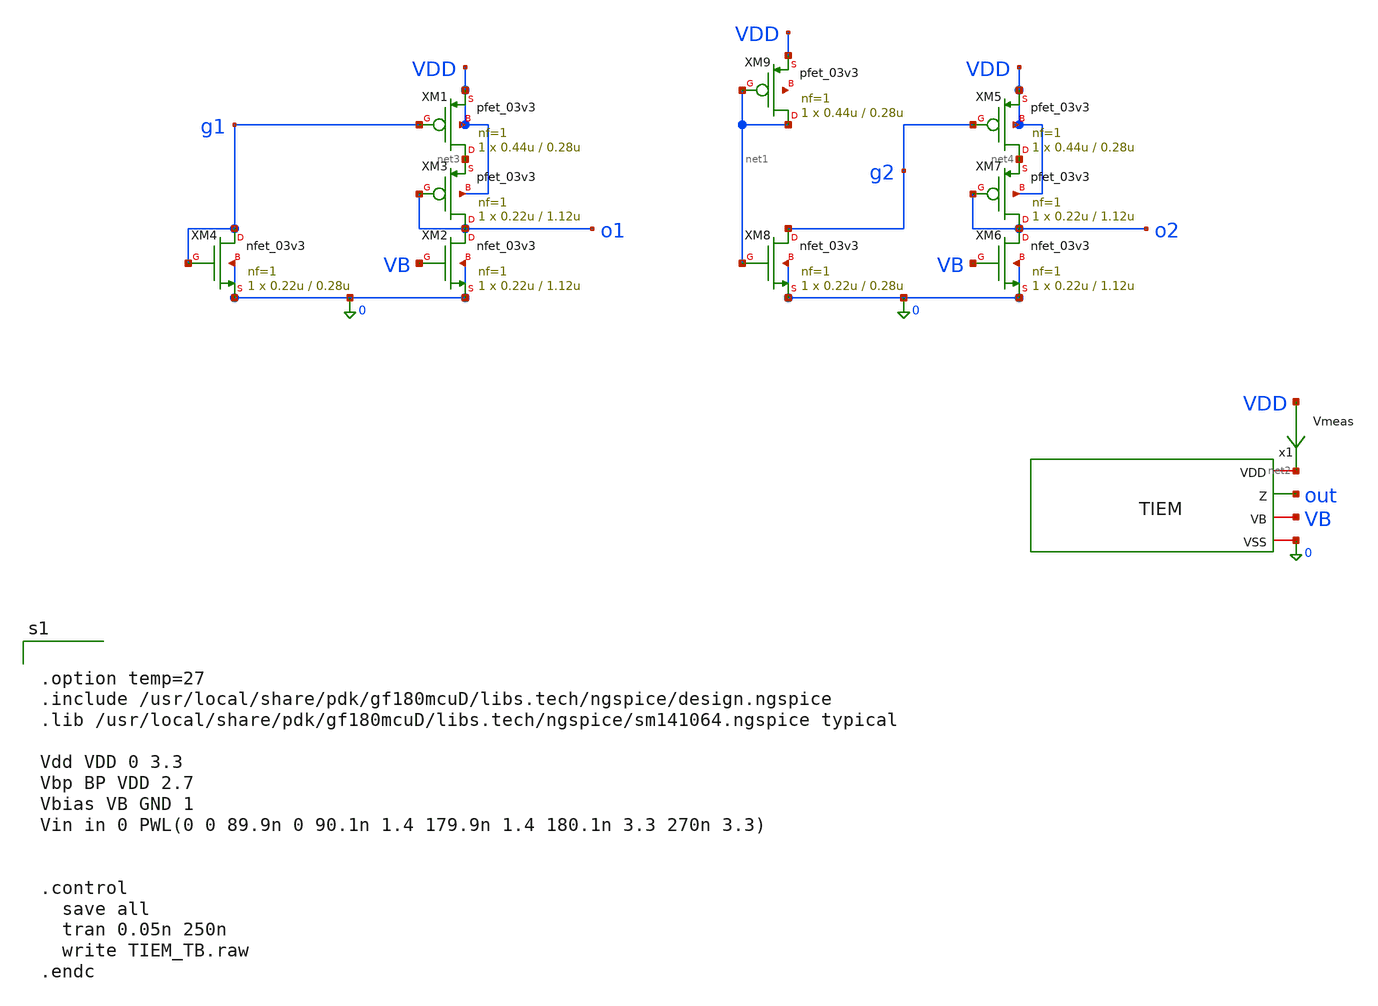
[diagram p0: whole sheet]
** sch_path: xschem_sn2/TIEM_TB.sch
**.subckt TIEM_TB
Vmeas VDD net2 0
.save i(vmeas)
x1 net2 out VB 0 TIEM
XM1 net3 g1 VDD VDD pfet_03v3 L=0.28u W=0.44u nf=1 ad='int((nf+1)/2) * W/nf * 0.18u' as='int((nf+2)/2) * W/nf * 0.18u'
+ pd='2*int((nf+1)/2) * (W/nf + 0.18u)' ps='2*int((nf+2)/2) * (W/nf + 0.18u)' nrd='0.18u / W' nrs='0.18u / W'
+ sa=0 sb=0 sd=0 m=1 par=1
XM2 o1 VB 0 0 nfet_03v3 L=1.12u W=0.22u nf=1 ad='int((nf+1)/2) * W/nf * 0.18u' as='int((nf+2)/2) * W/nf * 0.18u'
+ pd='2*int((nf+1)/2) * (W/nf + 0.18u)' ps='2*int((nf+2)/2) * (W/nf + 0.18u)' nrd='0.18u / W' nrs='0.18u / W'
+ sa=0 sb=0 sd=0 m=1 par=1
XM3 o1 o1 net3 VDD pfet_03v3 L=1.12u W=0.22u nf=1 ad='int((nf+1)/2) * W/nf * 0.18u' as='int((nf+2)/2) * W/nf * 0.18u'
+ pd='2*int((nf+1)/2) * (W/nf + 0.18u)' ps='2*int((nf+2)/2) * (W/nf + 0.18u)' nrd='0.18u / W' nrs='0.18u / W'
+ sa=0 sb=0 sd=0 m=1 par=1
XM4 g1 g1 0 0 nfet_03v3 L=0.28u W=0.22u nf=1 ad='int((nf+1)/2) * W/nf * 0.18u' as='int((nf+2)/2) * W/nf * 0.18u'
+ pd='2*int((nf+1)/2) * (W/nf + 0.18u)' ps='2*int((nf+2)/2) * (W/nf + 0.18u)' nrd='0.18u / W' nrs='0.18u / W'
+ sa=0 sb=0 sd=0 m=1 par=1
XM5 net4 g2 VDD VDD pfet_03v3 L=0.28u W=0.44u nf=1 ad='int((nf+1)/2) * W/nf * 0.18u' as='int((nf+2)/2) * W/nf * 0.18u'
+ pd='2*int((nf+1)/2) * (W/nf + 0.18u)' ps='2*int((nf+2)/2) * (W/nf + 0.18u)' nrd='0.18u / W' nrs='0.18u / W'
+ sa=0 sb=0 sd=0 m=1 par=1
XM6 o2 VB 0 0 nfet_03v3 L=1.12u W=0.22u nf=1 ad='int((nf+1)/2) * W/nf * 0.18u' as='int((nf+2)/2) * W/nf * 0.18u'
+ pd='2*int((nf+1)/2) * (W/nf + 0.18u)' ps='2*int((nf+2)/2) * (W/nf + 0.18u)' nrd='0.18u / W' nrs='0.18u / W'
+ sa=0 sb=0 sd=0 m=1 par=1
XM7 o2 o2 net4 VDD pfet_03v3 L=1.12u W=0.22u nf=1 ad='int((nf+1)/2) * W/nf * 0.18u' as='int((nf+2)/2) * W/nf * 0.18u'
+ pd='2*int((nf+1)/2) * (W/nf + 0.18u)' ps='2*int((nf+2)/2) * (W/nf + 0.18u)' nrd='0.18u / W' nrs='0.18u / W'
+ sa=0 sb=0 sd=0 m=1 par=1
XM8 g2 net1 0 0 nfet_03v3 L=0.28u W=0.22u nf=1 ad='int((nf+1)/2) * W/nf * 0.18u' as='int((nf+2)/2) * W/nf * 0.18u'
+ pd='2*int((nf+1)/2) * (W/nf + 0.18u)' ps='2*int((nf+2)/2) * (W/nf + 0.18u)' nrd='0.18u / W' nrs='0.18u / W'
+ sa=0 sb=0 sd=0 m=1 par=1
XM9 net1 net1 VDD net5 pfet_03v3 L=0.28u W=0.44u nf=1 ad='int((nf+1)/2) * W/nf * 0.18u' as='int((nf+2)/2) * W/nf * 0.18u'
+ pd='2*int((nf+1)/2) * (W/nf + 0.18u)' ps='2*int((nf+2)/2) * (W/nf + 0.18u)' nrd='0.18u / W' nrs='0.18u / W'
+ sa=0 sb=0 sd=0 m=1 par=1
**** begin user architecture code


.option temp=27
.include /usr/local/share/pdk/gf180mcuD/libs.tech/ngspice/design.ngspice
.lib /usr/local/share/pdk/gf180mcuD/libs.tech/ngspice/sm141064.ngspice typical

Vdd VDD 0 3.3
Vbp BP VDD 2.7
Vbias VB GND 1
Vin in 0 PWL(0 0 89.9n 0 90.1n 1.4 179.9n 1.4 180.1n 3.3 270n 3.3)


.control
  save all
  tran 0.05n 250n
  write TIEM_TB.raw
.endc


**** end user architecture code
**.ends

* expanding   symbol:  xschem_sn2/TIEM.sym # of pins=4
** sym_path: xschem_sn2/TIEM.sym
** sch_path: xschem_sn2/TIEM.sch
.subckt TIEM VDD Z VB VSS
*.iopin VSS
*.iopin VDD
*.opin Z
*.iopin VB
XM1 net2 net1 VDD VDD pfet_03v3 L=0.28u W=0.44u nf=1 ad='int((nf+1)/2) * W/nf * 0.18u' as='int((nf+2)/2) * W/nf * 0.18u'
+ pd='2*int((nf+1)/2) * (W/nf + 0.18u)' ps='2*int((nf+2)/2) * (W/nf + 0.18u)' nrd='0.18u / W' nrs='0.18u / W'
+ sa=0 sb=0 sd=0 m=1 par=1
XM2 Z VB VSS VSS nfet_03v3 L=1.12u W=0.22u nf=1 ad='int((nf+1)/2) * W/nf * 0.18u' as='int((nf+2)/2) * W/nf * 0.18u'
+ pd='2*int((nf+1)/2) * (W/nf + 0.18u)' ps='2*int((nf+2)/2) * (W/nf + 0.18u)' nrd='0.18u / W' nrs='0.18u / W'
+ sa=0 sb=0 sd=0 m=1 par=1
XM3 Z Z net2 VDD pfet_03v3 L=1.12u W=0.22u nf=1 ad='int((nf+1)/2) * W/nf * 0.18u' as='int((nf+2)/2) * W/nf * 0.18u'
+ pd='2*int((nf+1)/2) * (W/nf + 0.18u)' ps='2*int((nf+2)/2) * (W/nf + 0.18u)' nrd='0.18u / W' nrs='0.18u / W'
+ sa=0 sb=0 sd=0 m=1 par=1
XM4 net1 net1 VSS VSS nfet_03v3 L=0.28u W=0.22u nf=1 ad='int((nf+1)/2) * W/nf * 0.18u' as='int((nf+2)/2) * W/nf * 0.18u'
+ pd='2*int((nf+1)/2) * (W/nf + 0.18u)' ps='2*int((nf+2)/2) * (W/nf + 0.18u)' nrd='0.18u / W' nrs='0.18u / W'
+ sa=0 sb=0 sd=0 m=1 par=1
.ends

.end
